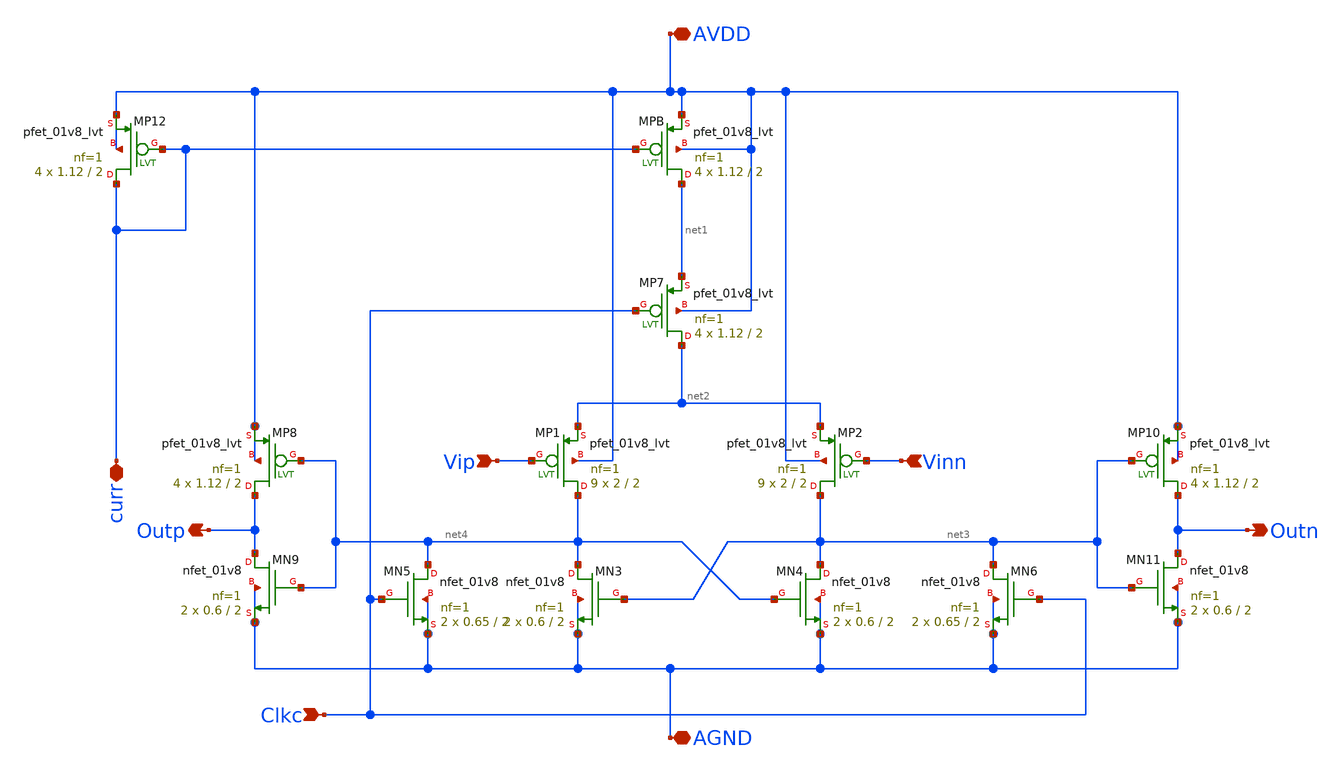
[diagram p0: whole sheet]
** sch_path: sar-adc/updated/Dynamic_Comparator.sch
**.subckt Dynamic_Comparator Vip Vinn Outn Outp Clkc AVDD AGND curr
*.ipin Vip
*.ipin Vinn
*.opin Outn
*.opin Outp
*.ipin Clkc
*.iopin AVDD
*.iopin AGND
*.iopin curr
XMPB net1 curr AVDD AVDD sky130_fd_pr__pfet_01v8_lvt L=2 W=1.12 nf=1 ad='int((1 + 1)/2) * 1.12 / 1 * 0.29'
+ as='int((1 + 2)/2) * 1.12 / 1 * 0.29' pd='2*int((1 + 1)/2) * (1.12 / 1 + 0.29)' ps='2*int((1 + 2)/2) * (1.12 / 1 + 0.29)'
+ nrd='0.29 / 1.12 ' nrs='0.29 / 1.12 ' sa=0 sb=0 sd=0 mult=4 m=4
XMP7 net2 Clkc net1 AVDD sky130_fd_pr__pfet_01v8_lvt L=2 W=1.12 nf=1 ad='int((1 + 1)/2) * 1.12 / 1 * 0.29'
+ as='int((1 + 2)/2) * 1.12 / 1 * 0.29' pd='2*int((1 + 1)/2) * (1.12 / 1 + 0.29)' ps='2*int((1 + 2)/2) * (1.12 / 1 + 0.29)'
+ nrd='0.29 / 1.12 ' nrs='0.29 / 1.12 ' sa=0 sb=0 sd=0 mult=4 m=4
XMP12 curr curr AVDD AVDD sky130_fd_pr__pfet_01v8_lvt L=2 W=1.12 nf=1 ad='int((1 + 1)/2) * 1.12 / 1 * 0.29'
+ as='int((1 + 2)/2) * 1.12 / 1 * 0.29' pd='2*int((1 + 1)/2) * (1.12 / 1 + 0.29)' ps='2*int((1 + 2)/2) * (1.12 / 1 + 0.29)'
+ nrd='0.29 / 1.12 ' nrs='0.29 / 1.12 ' sa=0 sb=0 sd=0 mult=4 m=4
XMP1 net4 Vip net2 AVDD sky130_fd_pr__pfet_01v8_lvt L=2 W=2 nf=1 ad='int((1 + 1)/2) * 2 / 1 * 0.29' as='int((1 + 2)/2) * 2 / 1 * 0.29'
+ pd='2*int((1 + 1)/2) * (2 / 1 + 0.29)' ps='2*int((1 + 2)/2) * (2 / 1 + 0.29)' nrd='0.29 / 2 ' nrs='0.29 / 2 '
+ sa=0 sb=0 sd=0 mult=9 m=9
XMP2 net3 Vinn net2 AVDD sky130_fd_pr__pfet_01v8_lvt L=2 W=2 nf=1 ad='int((1 + 1)/2) * 2 / 1 * 0.29'
+ as='int((1 + 2)/2) * 2 / 1 * 0.29' pd='2*int((1 + 1)/2) * (2 / 1 + 0.29)' ps='2*int((1 + 2)/2) * (2 / 1 + 0.29)'
+ nrd='0.29 / 2 ' nrs='0.29 / 2 ' sa=0 sb=0 sd=0 mult=9 m=9
XMP8 Outp net4 AVDD AVDD sky130_fd_pr__pfet_01v8_lvt L=2 W=1.12 nf=1 ad='int((1 + 1)/2) * 1.12 / 1 * 0.29'
+ as='int((1 + 2)/2) * 1.12 / 1 * 0.29' pd='2*int((1 + 1)/2) * (1.12 / 1 + 0.29)' ps='2*int((1 + 2)/2) * (1.12 / 1 + 0.29)'
+ nrd='0.29 / 1.12 ' nrs='0.29 / 1.12 ' sa=0 sb=0 sd=0 mult=4 m=4
XMP10 Outn net3 AVDD AVDD sky130_fd_pr__pfet_01v8_lvt L=2 W=1.12 nf=1 ad='int((1 + 1)/2) * 1.12 / 1 * 0.29'
+ as='int((1 + 2)/2) * 1.12 / 1 * 0.29' pd='2*int((1 + 1)/2) * (1.12 / 1 + 0.29)' ps='2*int((1 + 2)/2) * (1.12 / 1 + 0.29)'
+ nrd='0.29 / 1.12 ' nrs='0.29 / 1.12 ' sa=0 sb=0 sd=0 mult=4 m=4
XMN5 net4 Clkc AGND AGND sky130_fd_pr__nfet_01v8 L=2 W=0.65 nf=1 ad='int((1 + 1)/2) * 0.65 / 1 * 0.29'
+ as='int((1 + 2)/2) * 0.65 / 1 * 0.29' pd='2*int((1 + 1)/2) * (0.65 / 1 + 0.29)' ps='2*int((1 + 2)/2) * (0.65 / 1 + 0.29)'
+ nrd='0.29 / 0.65 ' nrs='0.29 / 0.65 ' sa=0 sb=0 sd=0 mult=2 m=2
XMN3 net4 net3 AGND AGND sky130_fd_pr__nfet_01v8 L=2 W=0.6 nf=1 ad='int((1 + 1)/2) * 0.6 / 1 * 0.29'
+ as='int((1 + 2)/2) * 0.6 / 1 * 0.29' pd='2*int((1 + 1)/2) * (0.6 / 1 + 0.29)' ps='2*int((1 + 2)/2) * (0.6 / 1 + 0.29)'
+ nrd='0.29 / 0.6 ' nrs='0.29 / 0.6 ' sa=0 sb=0 sd=0 mult=2 m=2
XMN4 net3 net4 AGND AGND sky130_fd_pr__nfet_01v8 L=2 W=0.6 nf=1 ad='int((1 + 1)/2) * 0.6 / 1 * 0.29'
+ as='int((1 + 2)/2) * 0.6 / 1 * 0.29' pd='2*int((1 + 1)/2) * (0.6 / 1 + 0.29)' ps='2*int((1 + 2)/2) * (0.6 / 1 + 0.29)'
+ nrd='0.29 / 0.6 ' nrs='0.29 / 0.6 ' sa=0 sb=0 sd=0 mult=2 m=2
XMN6 net3 Clkc AGND AGND sky130_fd_pr__nfet_01v8 L=2 W=0.65 nf=1 ad='int((1 + 1)/2) * 0.65 / 1 * 0.29'
+ as='int((1 + 2)/2) * 0.65 / 1 * 0.29' pd='2*int((1 + 1)/2) * (0.65 / 1 + 0.29)' ps='2*int((1 + 2)/2) * (0.65 / 1 + 0.29)'
+ nrd='0.29 / 0.65 ' nrs='0.29 / 0.65 ' sa=0 sb=0 sd=0 mult=2 m=2
XMN9 Outp net4 AGND AGND sky130_fd_pr__nfet_01v8 L=2 W=0.6 nf=1 ad='int((1 + 1)/2) * 0.6 / 1 * 0.29'
+ as='int((1 + 2)/2) * 0.6 / 1 * 0.29' pd='2*int((1 + 1)/2) * (0.6 / 1 + 0.29)' ps='2*int((1 + 2)/2) * (0.6 / 1 + 0.29)'
+ nrd='0.29 / 0.6 ' nrs='0.29 / 0.6 ' sa=0 sb=0 sd=0 mult=2 m=2
XMN11 Outn net3 AGND AGND sky130_fd_pr__nfet_01v8 L=2 W=0.6 nf=1 ad='int((1 + 1)/2) * 0.6 / 1 * 0.29'
+ as='int((1 + 2)/2) * 0.6 / 1 * 0.29' pd='2*int((1 + 1)/2) * (0.6 / 1 + 0.29)' ps='2*int((1 + 2)/2) * (0.6 / 1 + 0.29)'
+ nrd='0.29 / 0.6 ' nrs='0.29 / 0.6 ' sa=0 sb=0 sd=0 mult=2 m=2
**.ends
.end
